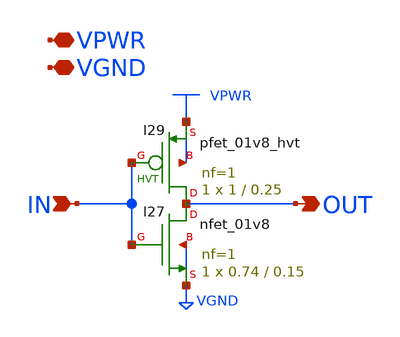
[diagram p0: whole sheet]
** sch_path: gpiov2_amux_ctl_inv_1.sch
* Copyright 2023 David Mitchell Bailey
* Licensed under the Apache License, Version 2.0 (the "License");
* you may not use this file except in compliance with the License.
* You may obtain a copy of the License at
* https://www.apache.org/licenses/LICENSE-2.0
* Unless required by applicable law or agreed to in writing, software
* distributed under the License is distributed on an "AS IS" BASIS,
* WITHOUT WARRANTIES OR CONDITIONS OF ANY KIND, either express or implied.
* See the License for the specific language governing permissions and
* limitations under the License.
**.subckt gpiov2_amux_ctl_inv_1 IN OUT VPWR VGND
*.ipin IN
*.opin OUT
*.iopin VPWR
*.iopin VGND
XI27 OUT IN VGND VGND sky130_fd_pr__nfet_01v8 L=0.15 W=0.74 nf=1 ad='int((nf+1)/2) * W/nf * 0.29' as='int((nf+2)/2) * W/nf * 0.29'
+ pd='2*int((nf+1)/2) * (W/nf + 0.29)' ps='2*int((nf+2)/2) * (W/nf + 0.29)' nrd='0.29 / W' nrs='0.29 / W'
+ sa=0 sb=0 sd=0 mult=1 m=1
XI29 OUT IN VPWR VPWR sky130_fd_pr__pfet_01v8_hvt L=0.25 W=1 nf=1 ad='int((nf+1)/2) * W/nf * 0.29' as='int((nf+2)/2) * W/nf * 0.29'
+ pd='2*int((nf+1)/2) * (W/nf + 0.29)' ps='2*int((nf+2)/2) * (W/nf + 0.29)' nrd='0.29 / W' nrs='0.29 / W'
+ sa=0 sb=0 sd=0 mult=1 m=1
**.ends
.end
